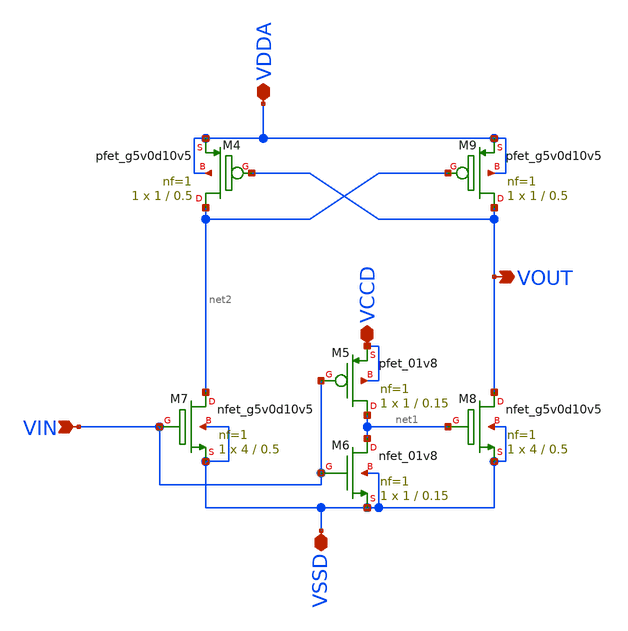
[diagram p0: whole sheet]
** sch_path: Layout_v2/All_schematic/level_tx_1bit.sch
**.subckt level_tx_1bit VDDA VIN VOUT VCCD VSSD
*.iopin VDDA
*.ipin VIN
*.opin VOUT
*.iopin VCCD
*.iopin VSSD
XM4 net2 VOUT VDDA VDDA sky130_fd_pr__pfet_g5v0d10v5 L=0.5 W=1 nf=1 ad='int((nf+1)/2) * W/nf * 0.29'
+ as='int((nf+2)/2) * W/nf * 0.29' pd='2*int((nf+1)/2) * (W/nf + 0.29)' ps='2*int((nf+2)/2) * (W/nf + 0.29)'
+ nrd='0.29 / W' nrs='0.29 / W' sa=0 sb=0 sd=0 mult=1 m=1
XM5 net1 VIN VCCD VCCD sky130_fd_pr__pfet_01v8 L=0.15 W=1 nf=1 ad='int((nf+1)/2) * W/nf * 0.29' as='int((nf+2)/2) * W/nf * 0.29'
+ pd='2*int((nf+1)/2) * (W/nf + 0.29)' ps='2*int((nf+2)/2) * (W/nf + 0.29)' nrd='0.29 / W' nrs='0.29 / W'
+ sa=0 sb=0 sd=0 mult=1 m=1
XM6 net1 VIN VSSD VSSD sky130_fd_pr__nfet_01v8 L=0.15 W=1 nf=1 ad='int((nf+1)/2) * W/nf * 0.29' as='int((nf+2)/2) * W/nf * 0.29'
+ pd='2*int((nf+1)/2) * (W/nf + 0.29)' ps='2*int((nf+2)/2) * (W/nf + 0.29)' nrd='0.29 / W' nrs='0.29 / W'
+ sa=0 sb=0 sd=0 mult=1 m=1
XM7 net2 VIN VSSD VSSD sky130_fd_pr__nfet_g5v0d10v5 L=0.5 W=4 nf=1 ad='int((nf+1)/2) * W/nf * 0.29' as='int((nf+2)/2) * W/nf * 0.29'
+ pd='2*int((nf+1)/2) * (W/nf + 0.29)' ps='2*int((nf+2)/2) * (W/nf + 0.29)' nrd='0.29 / W' nrs='0.29 / W'
+ sa=0 sb=0 sd=0 mult=1 m=1
XM8 VOUT net1 VSSD VSSD sky130_fd_pr__nfet_g5v0d10v5 L=0.5 W=4 nf=1 ad='int((nf+1)/2) * W/nf * 0.29'
+ as='int((nf+2)/2) * W/nf * 0.29' pd='2*int((nf+1)/2) * (W/nf + 0.29)' ps='2*int((nf+2)/2) * (W/nf + 0.29)'
+ nrd='0.29 / W' nrs='0.29 / W' sa=0 sb=0 sd=0 mult=1 m=1
XM9 VOUT net2 VDDA VDDA sky130_fd_pr__pfet_g5v0d10v5 L=0.5 W=1 nf=1 ad='int((nf+1)/2) * W/nf * 0.29'
+ as='int((nf+2)/2) * W/nf * 0.29' pd='2*int((nf+1)/2) * (W/nf + 0.29)' ps='2*int((nf+2)/2) * (W/nf + 0.29)'
+ nrd='0.29 / W' nrs='0.29 / W' sa=0 sb=0 sd=0 mult=1 m=1
**.ends
.end
